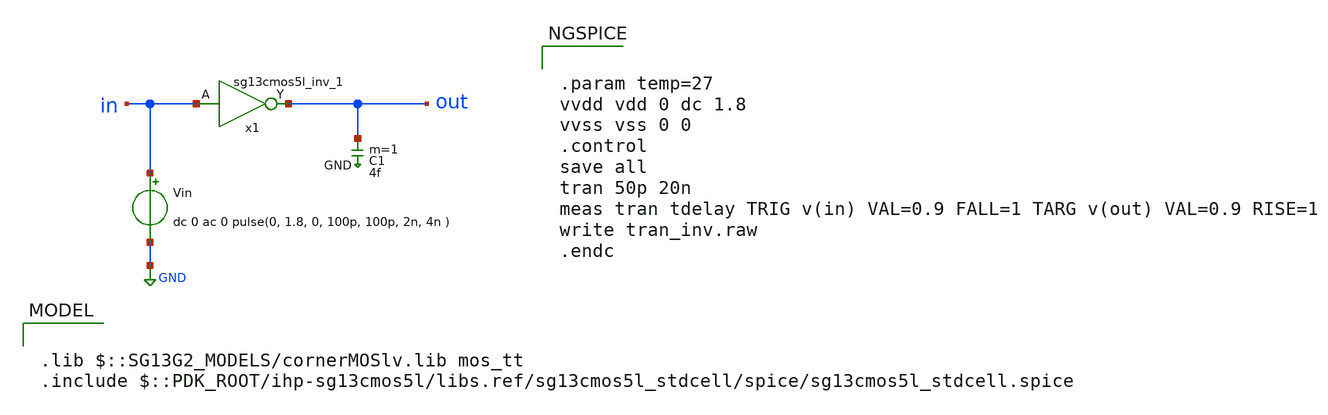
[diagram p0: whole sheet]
** sch_path: ihp-sg13cmos5l/libs.tech/xschem/sg13cmos5l_stdcells/tran_inv.sch
* Copyright 2024 IHP PDK Authors

.lib $::SG13G2_MODELS/cornerMOSlv.lib mos_tt
.include $::PDK_ROOT/ihp-sg13cmos5l/libs.ref/sg13cmos5l_stdcell/spice/sg13cmos5l_stdcell.spice

**.subckt tran_inv
Vin in GND dc 0 ac 0 pulse(0, 1.8, 0, 100p, 100p, 2n, 4n )
x1 out in VDD VSS sg13cmos5l_inv_1
C1 out GND 4f m=1
**** begin user architecture code


.param temp=27
vvdd vdd 0 dc 1.8
vvss vss 0 0
.control
save all
tran 50p 20n
meas tran tdelay TRIG v(in) VAL=0.9 FALL=1 TARG v(out) VAL=0.9 RISE=1
write tran_inv.raw
.endc


**** end user architecture code
**.ends
.GLOBAL GND
.end
